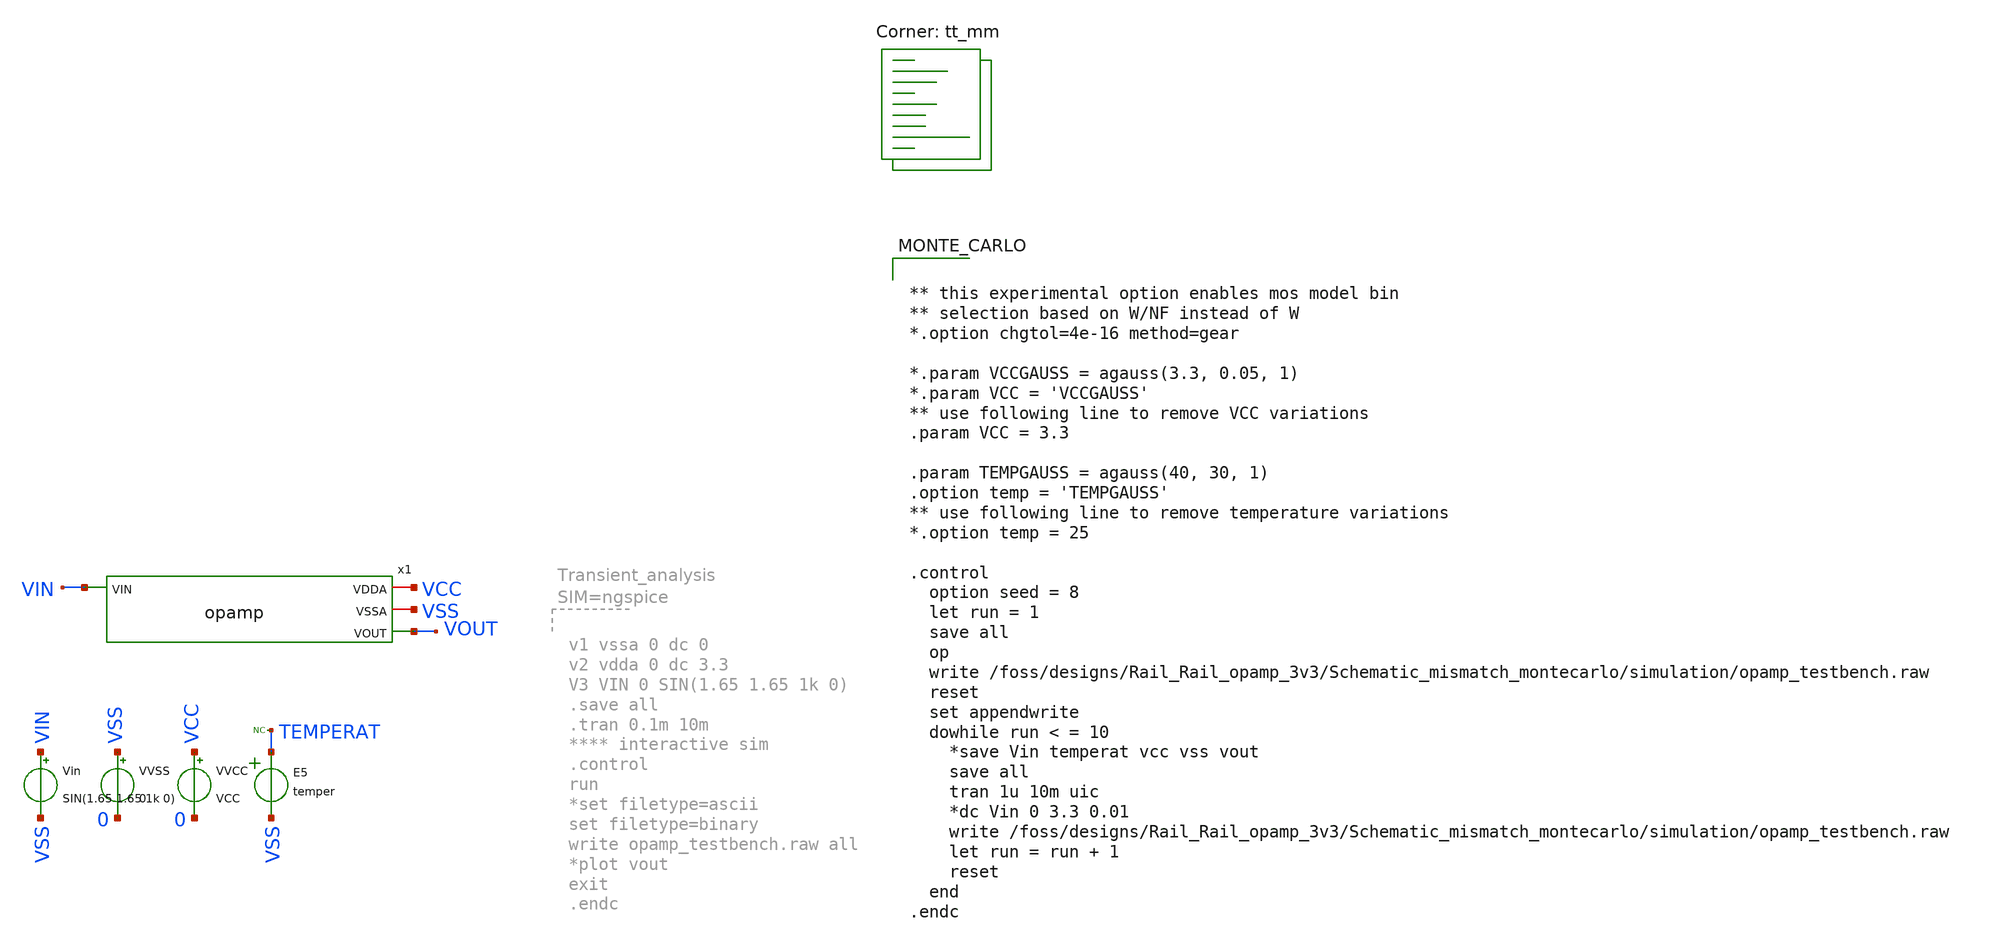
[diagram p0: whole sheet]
** sch_path: Rail_Rail_opamp_3v3/Schematic_mismatch_montecarlo/opamp_testbench.sch
**.subckt opamp_testbench
x1 VCC VSS VIN VOUT opamp
Vin VIN VSS SIN(1.65 1.65 1k 0)
VVSS VSS 0 0
VVCC VCC 0 VCC
E5 TEMPERAT VSS VOL=' temper '
* noconn TEMPERAT
**** begin user architecture code


** this experimental option enables mos model bin
** selection based on W/NF instead of W
*.option chgtol=4e-16 method=gear

*.param VCCGAUSS = agauss(3.3, 0.05, 1)
*.param VCC = 'VCCGAUSS'
** use following line to remove VCC variations
.param VCC = 3.3

.param TEMPGAUSS = agauss(40, 30, 1)
.option temp = 'TEMPGAUSS'
** use following line to remove temperature variations
*.option temp = 25

.control
  option seed = 8
  let run = 1
  save all
  op
  write
+ /foss/designs/Rail_Rail_opamp_3v3/Schematic_mismatch_montecarlo/simulation/opamp_testbench.raw
  reset
  set appendwrite
  dowhile run < = 10
    *save Vin temperat vcc vss vout
    save all
    tran 1u 10m uic
    *dc Vin 0 3.3 0.01
    write
+ /foss/designs/Rail_Rail_opamp_3v3/Schematic_mismatch_montecarlo/simulation/opamp_testbench.raw
    let run = run + 1
    reset
  end
.endc


.lib $::SKYWATER_MODELS/sky130.lib.spice tt_mm
**** end user architecture code
**.ends
.end
